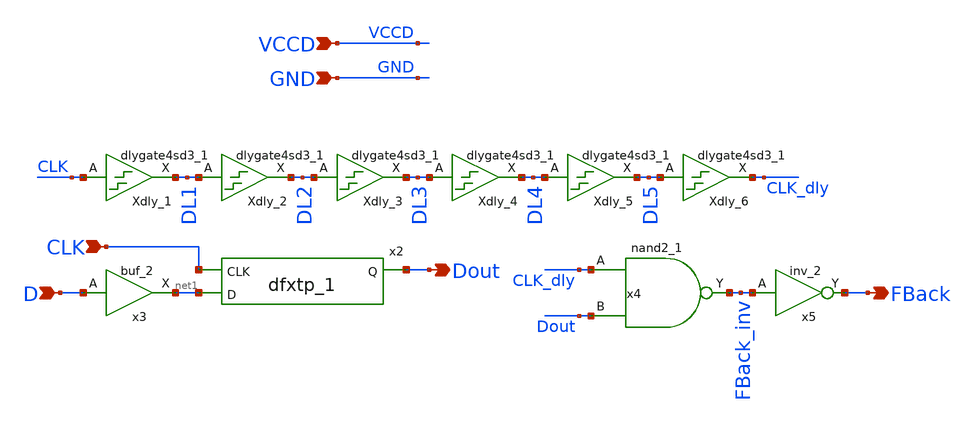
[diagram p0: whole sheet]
** sch_path: xschem/lib_qz/qz.sch
**.subckt qz CLK D Dout FBack VCCD GND
*.ipin CLK
*.ipin D
*.opin Dout
*.opin FBack
*.ipin VCCD
*.ipin GND
Xdly_1 CLK GND GND VCCD VCCD DL1 sky130_fd_sc_hd__dlygate4sd3_1
x2 CLK net1 GND GND VCCD VCCD Dout sky130_fd_sc_hd__dfxtp_1
x3 D GND GND VCCD VCCD net1 sky130_fd_sc_hd__buf_2
x4 CLK_dly Dout GND GND VCCD VCCD FBack_inv sky130_fd_sc_hd__nand2_1
x5 FBack_inv GND GND VCCD VCCD FBack sky130_fd_sc_hd__inv_2
Xdly_2 DL1 GND GND VCCD VCCD DL2 sky130_fd_sc_hd__dlygate4sd3_1
Xdly_3 DL2 GND GND VCCD VCCD DL3 sky130_fd_sc_hd__dlygate4sd3_1
Xdly_4 DL3 GND GND VCCD VCCD DL4 sky130_fd_sc_hd__dlygate4sd3_1
Xdly_5 DL4 GND GND VCCD VCCD DL5 sky130_fd_sc_hd__dlygate4sd3_1
Xdly_6 DL5 GND GND VCCD VCCD CLK_dly sky130_fd_sc_hd__dlygate4sd3_1
**.ends
.end
